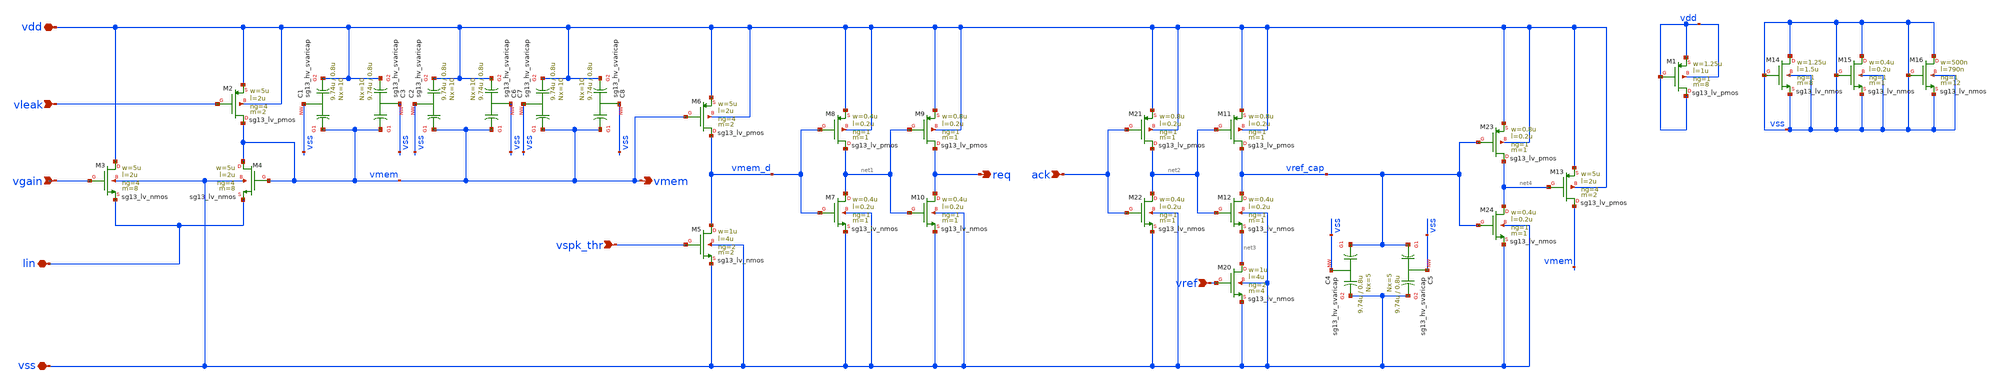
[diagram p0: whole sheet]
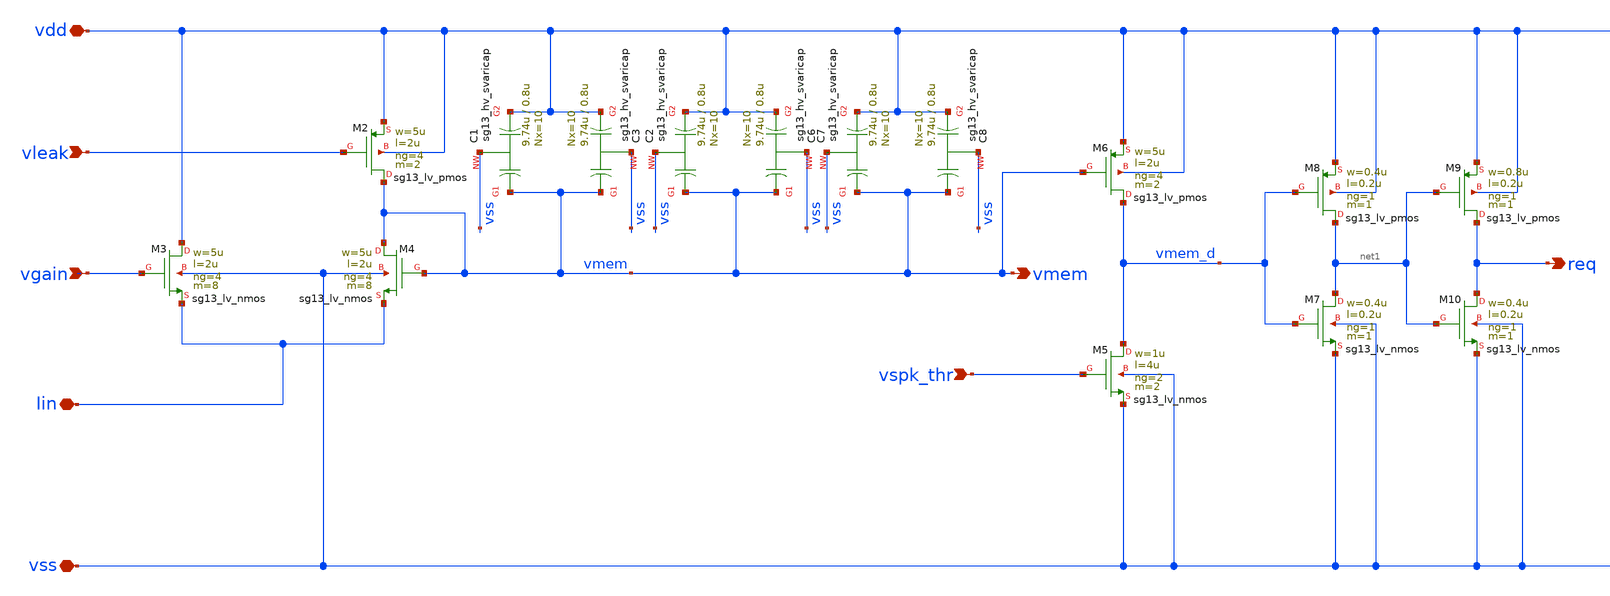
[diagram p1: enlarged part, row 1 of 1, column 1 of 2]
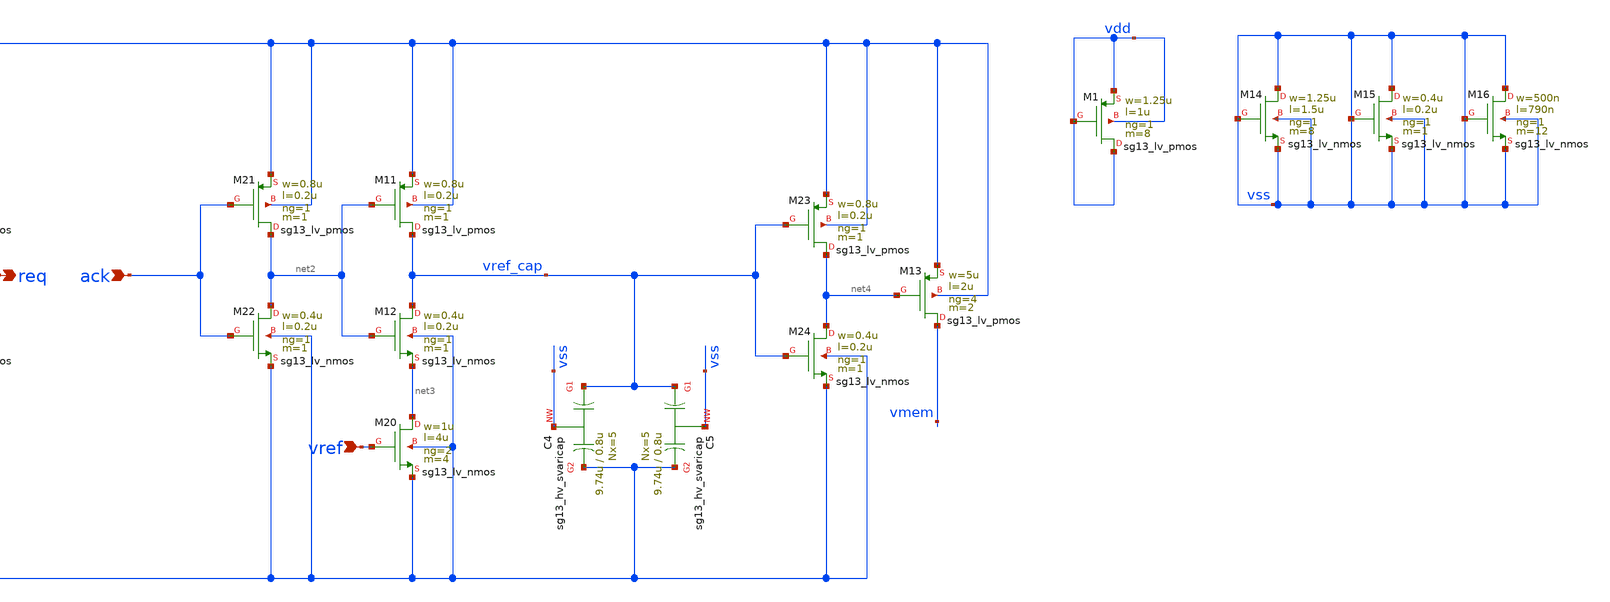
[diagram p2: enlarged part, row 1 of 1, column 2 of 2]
** sch_path: v2_feature_extr_withf/neuron_n_ADC.sch
**.subckt neuron_n_ADC vdd vss Iin vleak vspk_thr vref ack vmem req vgain
*.iopin vdd
*.iopin vss
*.iopin Iin
*.ipin vleak
*.ipin vspk_thr
*.ipin vref
*.ipin ack
*.opin vmem
*.opin req
*.ipin vgain
XM2 vmem vleak vdd vdd sg13_lv_pmos w=5u l=2u ng=4 m=2 mm_ok=1
XM3 vdd vgain Iin vss sg13_lv_nmos w=5u l=2u ng=4 m=8 mm_ok=1
XM4 vmem vmem Iin vss sg13_lv_nmos w=5u l=2u ng=4 m=8 mm_ok=1
XM5 vmem_d vspk_thr vss vss sg13_lv_nmos w=1u l=4u ng=2 m=2 mm_ok=1
XM6 vmem_d vmem vdd vdd sg13_lv_pmos w=5u l=2u ng=4 m=2 mm_ok=1
XM7 net1 vmem_d vss vss sg13_lv_nmos w=0.4u l=0.2u ng=1 m=1 mm_ok=1
XM8 net1 vmem_d vdd vdd sg13_lv_pmos w=0.4u l=0.2u ng=1 m=1 mm_ok=1
XM9 req net1 vdd vdd sg13_lv_pmos w=0.8u l=0.2u ng=1 m=1 mm_ok=1
XM10 req net1 vss vss sg13_lv_nmos w=0.4u l=0.2u ng=1 m=1 mm_ok=1
XM11 vref_cap net2 vdd vdd sg13_lv_pmos w=0.8u l=0.2u ng=1 m=1 mm_ok=1
XM12 vref_cap net2 net3 vss sg13_lv_nmos w=0.4u l=0.2u ng=1 m=1 mm_ok=1
XM13 vmem net4 vdd vdd sg13_lv_pmos w=5u l=2u ng=4 m=2 mm_ok=1
XM20 net3 vref vss vss sg13_lv_nmos w=1u l=4u ng=2 m=4 mm_ok=1
XM21 net2 ack vdd vdd sg13_lv_pmos w=0.8u l=0.2u ng=1 m=1 mm_ok=1
XM22 net2 ack vss vss sg13_lv_nmos w=0.4u l=0.2u ng=1 m=1 mm_ok=1
XM23 net4 vref_cap vdd vdd sg13_lv_pmos w=0.8u l=0.2u ng=1 m=1 mm_ok=1
XM24 net4 vref_cap vss vss sg13_lv_nmos w=0.4u l=0.2u ng=1 m=1 mm_ok=1
XC1 vmem vss vdd sub! sg13_hv_svaricap w=9.74u l=0.8u Nx=10 mm_ok=1
XC3 vmem vss vdd sub! sg13_hv_svaricap w=9.74u l=0.8u Nx=10 mm_ok=1
XC4 vref_cap vss vss sub! sg13_hv_svaricap w=9.74u l=0.8u Nx=5 mm_ok=1
XC5 vref_cap vss vss sub! sg13_hv_svaricap w=9.74u l=0.8u Nx=5 mm_ok=1
XC2 vmem vss vdd sub! sg13_hv_svaricap w=9.74u l=0.8u Nx=10 mm_ok=1
XC6 vmem vss vdd sub! sg13_hv_svaricap w=9.74u l=0.8u Nx=10 mm_ok=1
XC7 vmem vss vdd sub! sg13_hv_svaricap w=9.74u l=0.8u Nx=10 mm_ok=1
XC8 vmem vss vdd sub! sg13_hv_svaricap w=9.74u l=0.8u Nx=10 mm_ok=1
XM1 vdd vdd vdd vdd sg13_lv_pmos w=1.25u l=1u ng=1 m=8 mm_ok=1
XM14 vss vss vss vss sg13_lv_nmos w=1.25u l=1.5u ng=1 m=8 mm_ok=1
XM15 vss vss vss vss sg13_lv_nmos w=0.4u l=0.2u ng=1 m=1 mm_ok=1
XM16 vss vss vss vss sg13_lv_nmos w=500n l=790n ng=1 m=12 mm_ok=1
**.ends
.end
